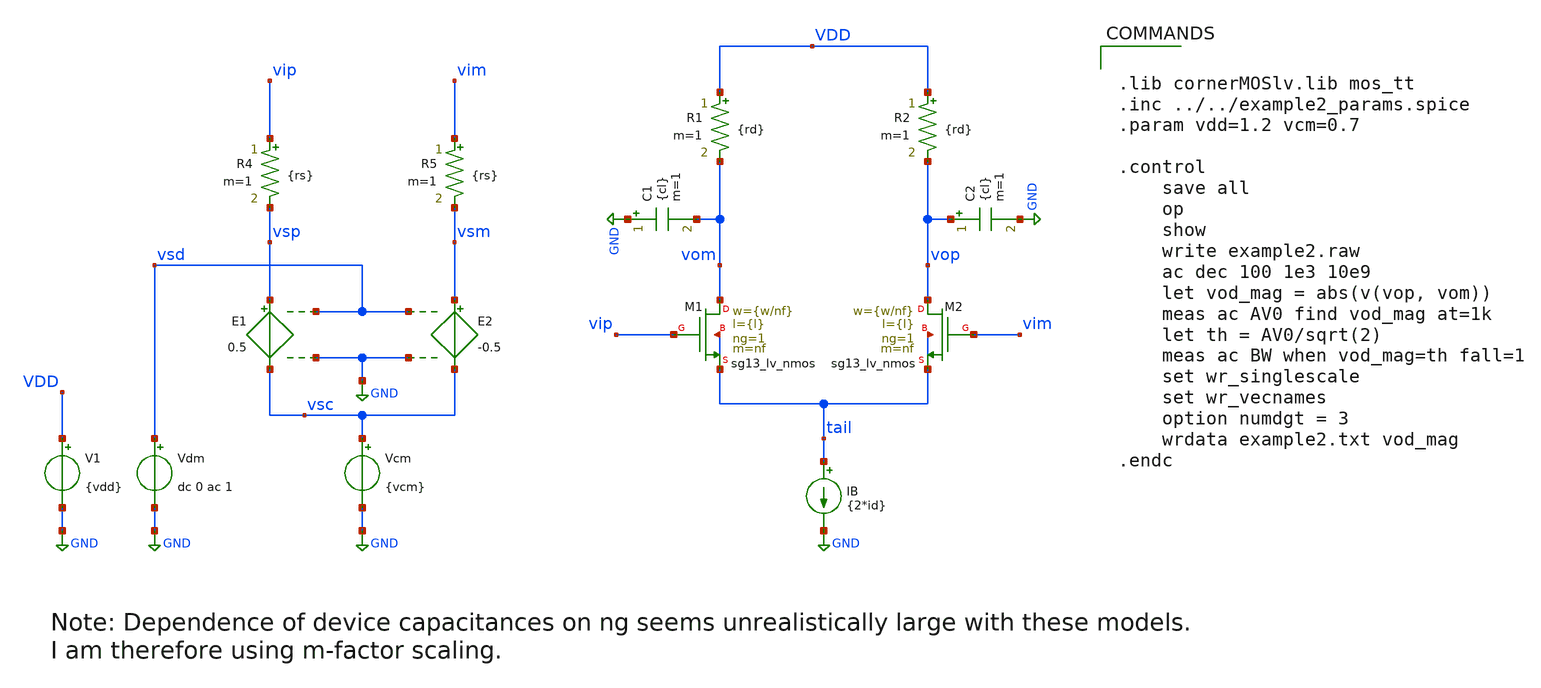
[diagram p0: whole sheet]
** sch_path: example2/xschem/example2.sch
**.subckt example2
E1 vsp vsc vsd GND 0.5
E2 vsm vsc vsd GND -0.5
Vdm vsd GND dc 0 ac 1
Vcm vsc GND {vcm}
V1 VDD GND {vdd}
IB tail GND {2*id}
XM1 vom vip tail tail sg13_lv_nmos w={w/nf} l={l} ng=1 m=nf mm_ok=1
XM2 vop vim tail tail sg13_lv_nmos w={w/nf} l={l} ng=1 m=nf mm_ok=1
R1 VDD vom {rd} m=1
R2 VDD vop {rd} m=1
R4 vip vsp {rs} m=1
R5 vim vsm {rs} m=1
C2 vop GND {cl} m=1
C1 GND vom {cl} m=1
**** begin user architecture code


.lib cornerMOSlv.lib mos_tt
.inc ../../example2_params.spice
.param vdd=1.2 vcm=0.7

.control
    save all
    op
    show
    write example2.raw
    ac dec 100 1e3 10e9
    let vod_mag = abs(v(vop, vom))
    meas ac AV0 find vod_mag at=1k
    let th = AV0/sqrt(2)
    meas ac BW when vod_mag=th fall=1
    set wr_singlescale
    set wr_vecnames
    option numdgt = 3
    wrdata example2.txt vod_mag
.endc


**** end user architecture code
**.ends
.GLOBAL GND
.end
